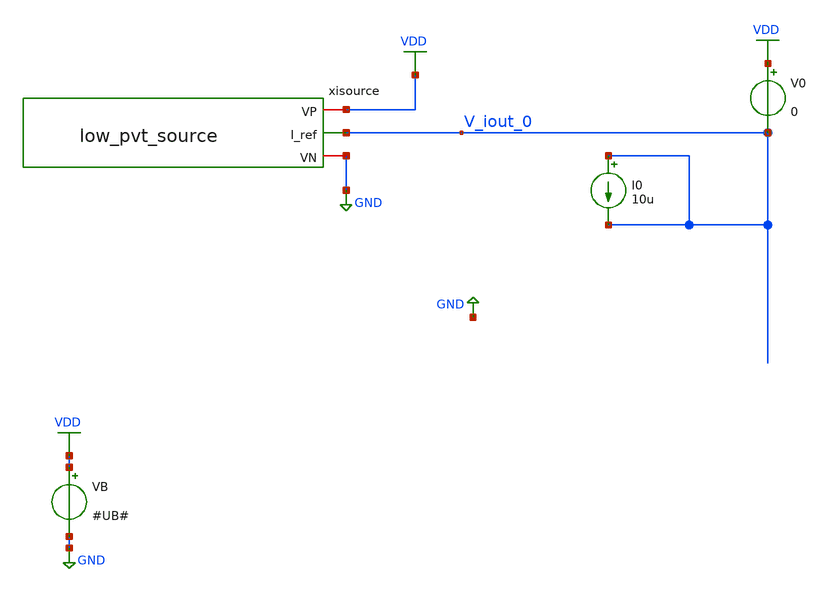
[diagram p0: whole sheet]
** sch_path: xschem/test/test_low_pvt_source_mc.sch
**.subckt test_low_pvt_source_mc
VB VDD GND #UB#
V0 VDD V_iout_0 0
xisource VDD V_iout_0 GND low_pvt_source
I0 V_iout_0 V_iout_0 10u
**** begin user architecture code


*.options savecurrents
.option warn=1
.control
set wr_vecnames
set wr_singlescale
set hcopydevtype=svg

set model="#model#"
let mc_runs=100
let mc_runNo = 1

dowhile mc_runNo <= mc_runs
   destroy all
	let min_temp=0
	let var_temp = min_temp
	let max_temp=100
	let temp_step=3
	dowhile var_temp <= max_temp
		option temp=$&var_temp
		wrdata 'result_op_op_{$&var_temp}deg_{$&mc_runNo}.csv' i(V0)
		op
		run
		if i(V0) > 1.3E-5
			echo 'Large current'
*			print i(v.xisource.v1) i(V0)
*			write 'result_op_high_{$&var_temp}deg_{$&mc_runNo}_{$&i(v.xisource.v1)}.raw'
		end
		if i(V0) < 0.7E-5
			echo 'Large current'
*			print i(v.xisource.v1) i(V0)
*			write 'result_op_low_{$&var_temp}deg_{$&mc_runNo}_{$&i(v.xisource.v1)}.raw'
		end
*
*		tran 100n 100u
*		MEAS tran isource AVG i(v.xisource.v1) from=50u to=100u
*		wrdata 'result_tran_{$&var_temp}deg_{$&mc_runNo}.csv' isource
		run
		let var_temp = var_temp + temp_step
	end
	let  mc_runNo = mc_runNo +1
	reset
end

.endc




* .include ../../tia.spice
* .include ../../filter_diff.spice
* .include ../../cmm_sense3.spice

* .include bandgap.spice
.include ../../../low_pvt_source.spice



.lib $::SKYWATER_MODELS/sky130.lib.spice #model#
* .lib $::SKYWATER_MODELS/sky130.lib.spice.#model#.red #model#
* .lib /home/simon/share/pdk/sky130A/libs.tech/ngspice/sky130.lib.spice.tt.red tt

**** end user architecture code
**.ends

* expanding   symbol:  /home/simon/code/asic/analog/bias/low_pvt_source.sym # of pins=3
** sym_path: xschem/bias/low_pvt_source.sym
** sch_path: xschem/bias/low_pvt_source.sch
.subckt low_pvt_source VP I_ref VN
*.iopin VP
*.opin I_ref
*.iopin VN
XM1 VM1D VM8D VP VP sky130_fd_pr__pfet_01v8 L=1 W=4 nf=1 ad='int((nf+1)/2) * W/nf * 0.29' as='int((nf+2)/2) * W/nf * 0.29'
+ pd='2*int((nf+1)/2) * (W/nf + 0.29)' ps='2*int((nf+2)/2) * (W/nf + 0.29)' nrd='0.29 / W' nrs='0.29 / W'
+ sa=0 sb=0 sd=0 mult=10 m=10
XM2 VM2D VM2D VN VN sky130_fd_pr__nfet_01v8 L=6 W=4 nf=1 ad='int((nf+1)/2) * W/nf * 0.29' as='int((nf+2)/2) * W/nf * 0.29'
+ pd='2*int((nf+1)/2) * (W/nf + 0.29)' ps='2*int((nf+2)/2) * (W/nf + 0.29)' nrd='0.29 / W' nrs='0.29 / W'
+ sa=0 sb=0 sd=0 mult=30 m=30
XM5 VM9D VM8D VM1D VP sky130_fd_pr__pfet_01v8 L=0.2 W=4 nf=1 ad='int((nf+1)/2) * W/nf * 0.29' as='int((nf+2)/2) * W/nf * 0.29'
+ pd='2*int((nf+1)/2) * (W/nf + 0.29)' ps='2*int((nf+2)/2) * (W/nf + 0.29)' nrd='0.29 / W' nrs='0.29 / W'
+ sa=0 sb=0 sd=0 mult=2 m=2
XM11 VM11D VM2D VM12D VN sky130_fd_pr__nfet_01v8 L=6 W=4 nf=1 ad='int((nf+1)/2) * W/nf * 0.29' as='int((nf+2)/2) * W/nf * 0.29'
+ pd='2*int((nf+1)/2) * (W/nf + 0.29)' ps='2*int((nf+2)/2) * (W/nf + 0.29)' nrd='0.29 / W' nrs='0.29 / W'
+ sa=0 sb=0 sd=0 mult=65 m=65
XM12 VM12D VM12G VN VN sky130_fd_pr__nfet_01v8 L=6 W=4 nf=1 ad='int((nf+1)/2) * W/nf * 0.29' as='int((nf+2)/2) * W/nf * 0.29'
+ pd='2*int((nf+1)/2) * (W/nf + 0.29)' ps='2*int((nf+2)/2) * (W/nf + 0.29)' nrd='0.29 / W' nrs='0.29 / W'
+ sa=0 sb=0 sd=0 mult=2 m=2
XM14 VM14D VM12G VN VN sky130_fd_pr__nfet_01v8 L=6 W=4 nf=1 ad='int((nf+1)/2) * W/nf * 0.29' as='int((nf+2)/2) * W/nf * 0.29'
+ pd='2*int((nf+1)/2) * (W/nf + 0.29)' ps='2*int((nf+2)/2) * (W/nf + 0.29)' nrd='0.29 / W' nrs='0.29 / W'
+ sa=0 sb=0 sd=0 mult=2 m=2
XM16 VM16D VM8D VP VP sky130_fd_pr__pfet_01v8 L=1 W=4 nf=1 ad='int((nf+1)/2) * W/nf * 0.29' as='int((nf+2)/2) * W/nf * 0.29'
+ pd='2*int((nf+1)/2) * (W/nf + 0.29)' ps='2*int((nf+2)/2) * (W/nf + 0.29)' nrd='0.29 / W' nrs='0.29 / W'
+ sa=0 sb=0 sd=0 mult=10 m=10
XM17 VM8D VM8D VM16D VP sky130_fd_pr__pfet_01v8 L=0.2 W=4 nf=1 ad='int((nf+1)/2) * W/nf * 0.29' as='int((nf+2)/2) * W/nf * 0.29'
+ pd='2*int((nf+1)/2) * (W/nf + 0.29)' ps='2*int((nf+2)/2) * (W/nf + 0.29)' nrd='0.29 / W' nrs='0.29 / W'
+ sa=0 sb=0 sd=0 mult=2 m=2
XM18 VM18D VM8D VP VP sky130_fd_pr__pfet_01v8 L=1 W=4 nf=1 ad='int((nf+1)/2) * W/nf * 0.29' as='int((nf+2)/2) * W/nf * 0.29'
+ pd='2*int((nf+1)/2) * (W/nf + 0.29)' ps='2*int((nf+2)/2) * (W/nf + 0.29)' nrd='0.29 / W' nrs='0.29 / W'
+ sa=0 sb=0 sd=0 mult=10*3*2 m=10*3*2
XM19 VM14D VM8D VM18D VP sky130_fd_pr__pfet_01v8 L=0.2 W=4 nf=1 ad='int((nf+1)/2) * W/nf * 0.29' as='int((nf+2)/2) * W/nf * 0.29'
+ pd='2*int((nf+1)/2) * (W/nf + 0.29)' ps='2*int((nf+2)/2) * (W/nf + 0.29)' nrd='0.29 / W' nrs='0.29 / W'
+ sa=0 sb=0 sd=0 mult=2*3*2 m=2*3*2
XM20 VM20D VM8D VP VP sky130_fd_pr__pfet_01v8 L=1 W=4 nf=1 ad='int((nf+1)/2) * W/nf * 0.29' as='int((nf+2)/2) * W/nf * 0.29'
+ pd='2*int((nf+1)/2) * (W/nf + 0.29)' ps='2*int((nf+2)/2) * (W/nf + 0.29)' nrd='0.29 / W' nrs='0.29 / W'
+ sa=0 sb=0 sd=0 mult=10*1*1 m=10*1*1
XM21 VM22D VM8D VM20D VP sky130_fd_pr__pfet_01v8 L=0.2 W=4 nf=1 ad='int((nf+1)/2) * W/nf * 0.29' as='int((nf+2)/2) * W/nf * 0.29'
+ pd='2*int((nf+1)/2) * (W/nf + 0.29)' ps='2*int((nf+2)/2) * (W/nf + 0.29)' nrd='0.29 / W' nrs='0.29 / W'
+ sa=0 sb=0 sd=0 mult=2*1*1 m=2*1*1
XM22 VM22D VM4S VM3D VN sky130_fd_pr__nfet_01v8 L=6 W=4 nf=1 ad='int((nf+1)/2) * W/nf * 0.29' as='int((nf+2)/2) * W/nf * 0.29'
+ pd='2*int((nf+1)/2) * (W/nf + 0.29)' ps='2*int((nf+2)/2) * (W/nf + 0.29)' nrd='0.29 / W' nrs='0.29 / W'
+ sa=0 sb=0 sd=0 mult=20 m=20
XM3 VM3D VM3G VN VN sky130_fd_pr__nfet_01v8 L=6 W=4 nf=1 ad='int((nf+1)/2) * W/nf * 0.29' as='int((nf+2)/2) * W/nf * 0.29'
+ pd='2*int((nf+1)/2) * (W/nf + 0.29)' ps='2*int((nf+2)/2) * (W/nf + 0.29)' nrd='0.29 / W' nrs='0.29 / W'
+ sa=0 sb=0 sd=0 mult=4 m=4
XM13 VP VM14D VM12G VM12G sky130_fd_pr__nfet_01v8_lvt L=0.15 W=4 nf=1 ad='int((nf+1)/2) * W/nf * 0.29'
+ as='int((nf+2)/2) * W/nf * 0.29' pd='2*int((nf+1)/2) * (W/nf + 0.29)' ps='2*int((nf+2)/2) * (W/nf + 0.29)'
+ nrd='0.29 / W' nrs='0.29 / W' sa=0 sb=0 sd=0 mult=20 m=20
XM4 I_ref VM22D VM4S VN sky130_fd_pr__nfet_01v8_lvt L=0.15 W=4 nf=1 ad='int((nf+1)/2) * W/nf * 0.29'
+ as='int((nf+2)/2) * W/nf * 0.29' pd='2*int((nf+1)/2) * (W/nf + 0.29)' ps='2*int((nf+2)/2) * (W/nf + 0.29)'
+ nrd='0.29 / W' nrs='0.29 / W' sa=0 sb=0 sd=0 mult=20 m=20
XM48 VM50D VM11D VP VP sky130_fd_pr__pfet_01v8 L=2 W=0.5 nf=1 ad='int((nf+1)/2) * W/nf * 0.29' as='int((nf+2)/2) * W/nf * 0.29'
+ pd='2*int((nf+1)/2) * (W/nf + 0.29)' ps='2*int((nf+2)/2) * (W/nf + 0.29)' nrd='0.29 / W' nrs='0.29 / W'
+ sa=0 sb=0 sd=0 mult=1 m=1
XM50 VM50D VM11D VN VN sky130_fd_pr__nfet_01v8_lvt L=0.2 W=4 nf=1 ad='int((nf+1)/2) * W/nf * 0.29' as='int((nf+2)/2) * W/nf * 0.29'
+ pd='2*int((nf+1)/2) * (W/nf + 0.29)' ps='2*int((nf+2)/2) * (W/nf + 0.29)' nrd='0.29 / W' nrs='0.29 / W'
+ sa=0 sb=0 sd=0 mult=10 m=10
XC3 VP VM8D sky130_fd_pr__cap_mim_m3_1 W=20 L=20 MF=1 m=1
XM8 VM8D VM9D VM11D VM11D sky130_fd_pr__nfet_01v8_lvt L=1 W=4 nf=1 ad='int((nf+1)/2) * W/nf * 0.29' as='int((nf+2)/2) * W/nf * 0.29'
+ pd='2*int((nf+1)/2) * (W/nf + 0.29)' ps='2*int((nf+2)/2) * (W/nf + 0.29)' nrd='0.29 / W' nrs='0.29 / W'
+ sa=0 sb=0 sd=0 mult=20 m=20
XM9 VM9D VM9D VM2D VM2D sky130_fd_pr__nfet_01v8_lvt L=1 W=4 nf=1 ad='int((nf+1)/2) * W/nf * 0.29' as='int((nf+2)/2) * W/nf * 0.29'
+ pd='2*int((nf+1)/2) * (W/nf + 0.29)' ps='2*int((nf+2)/2) * (W/nf + 0.29)' nrd='0.29 / W' nrs='0.29 / W'
+ sa=0 sb=0 sd=0 mult=20 m=20
XM10 VM8D VM50D VN VN sky130_fd_pr__nfet_01v8 L=2 W=0.5 nf=1 ad='int((nf+1)/2) * W/nf * 0.29' as='int((nf+2)/2) * W/nf * 0.29'
+ pd='2*int((nf+1)/2) * (W/nf + 0.29)' ps='2*int((nf+2)/2) * (W/nf + 0.29)' nrd='0.29 / W' nrs='0.29 / W'
+ sa=0 sb=0 sd=0 mult=1 m=1
XC4 VN VP sky130_fd_pr__cap_mim_m3_2 W=30 L=30 MF=1 m=1
XR7 net3 VM4S VN sky130_fd_pr__res_xhigh_po_1p41 L=10 mult=1 m=1
XR3 net4 net3 VN sky130_fd_pr__res_xhigh_po_1p41 L=10 mult=1 m=1
XR4 net2 net4 VN sky130_fd_pr__res_xhigh_po_1p41 L=10 mult=1 m=1
XR5 net1 net2 VN sky130_fd_pr__res_xhigh_po_1p41 L=10 mult=1 m=1
XR6 VN net1 VN sky130_fd_pr__res_xhigh_po_1p41 L=10 mult=1 m=1
XR8 net5 VM12G VN sky130_fd_pr__res_xhigh_po_1p41 L=10 mult=1 m=1
XR1 net5 VM3G VN sky130_fd_pr__res_xhigh_po_1p41 L=10 mult=1 m=1
XR2 net7 net6 VN sky130_fd_pr__res_xhigh_po_1p41 L=10 mult=1 m=1
XR9 VN net6 VN sky130_fd_pr__res_xhigh_po_1p41 L=10 mult=1 m=1
XR10 net11 net7 VN sky130_fd_pr__res_xhigh_po_1p41 L=10 mult=1 m=1
XR11 net12 net11 VN sky130_fd_pr__res_xhigh_po_1p41 L=10 mult=1 m=1
XR12 net8 net12 VN sky130_fd_pr__res_xhigh_po_1p41 L=10 mult=1 m=1
XR13 net10 VM3G VN sky130_fd_pr__res_xhigh_po_1p41 L=10 mult=1 m=1
XR14 net9 net10 VN sky130_fd_pr__res_xhigh_po_1p41 L=10 mult=1 m=1
XR15 net8 net9 VN sky130_fd_pr__res_xhigh_po_1p41 L=10 mult=1 m=1
XC1 VN VP sky130_fd_pr__cap_mim_m3_2 W=30 L=30 MF=1 m=1
.ends

.GLOBAL VDD
.GLOBAL GND
.end
